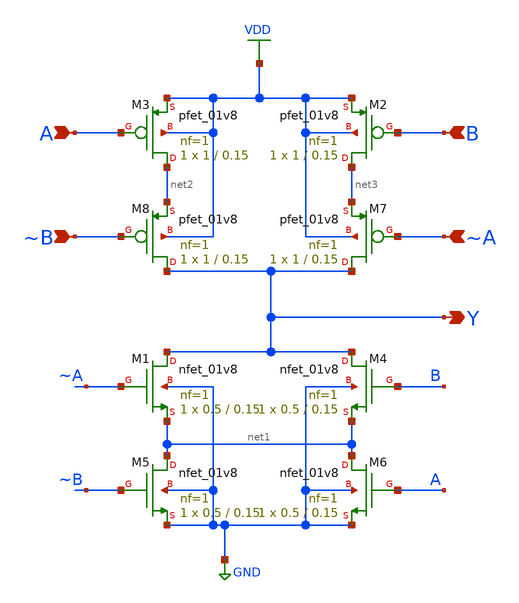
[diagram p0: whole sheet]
** sch_path: library/xschem/xor.sch
**.subckt xor Y A ~B B ~A
*.opin Y
*.ipin A
*.ipin ~B
*.ipin B
*.ipin ~A
XM1 Y ~A net1 GND sky130_fd_pr__nfet_01v8 L=0.15 W=0.5 nf=1 ad='int((nf+1)/2) * W/nf * 0.29' as='int((nf+2)/2) * W/nf * 0.29'
+ pd='2*int((nf+1)/2) * (W/nf + 0.29)' ps='2*int((nf+2)/2) * (W/nf + 0.29)' nrd='0.29 / W' nrs='0.29 / W'
+ sa=0 sb=0 sd=0 mult=1 m=1
XM2 net3 B VDD VDD sky130_fd_pr__pfet_01v8 L=0.15 W=1 nf=1 ad='int((nf+1)/2) * W/nf * 0.29' as='int((nf+2)/2) * W/nf * 0.29'
+ pd='2*int((nf+1)/2) * (W/nf + 0.29)' ps='2*int((nf+2)/2) * (W/nf + 0.29)' nrd='0.29 / W' nrs='0.29 / W'
+ sa=0 sb=0 sd=0 mult=1 m=1
XM3 net2 A VDD VDD sky130_fd_pr__pfet_01v8 L=0.15 W=1 nf=1 ad='int((nf+1)/2) * W/nf * 0.29' as='int((nf+2)/2) * W/nf * 0.29'
+ pd='2*int((nf+1)/2) * (W/nf + 0.29)' ps='2*int((nf+2)/2) * (W/nf + 0.29)' nrd='0.29 / W' nrs='0.29 / W'
+ sa=0 sb=0 sd=0 mult=1 m=1
XM4 Y B net1 GND sky130_fd_pr__nfet_01v8 L=0.15 W=0.5 nf=1 ad='int((nf+1)/2) * W/nf * 0.29' as='int((nf+2)/2) * W/nf * 0.29'
+ pd='2*int((nf+1)/2) * (W/nf + 0.29)' ps='2*int((nf+2)/2) * (W/nf + 0.29)' nrd='0.29 / W' nrs='0.29 / W'
+ sa=0 sb=0 sd=0 mult=1 m=1
XM5 net1 ~B GND GND sky130_fd_pr__nfet_01v8 L=0.15 W=0.5 nf=1 ad='int((nf+1)/2) * W/nf * 0.29' as='int((nf+2)/2) * W/nf * 0.29'
+ pd='2*int((nf+1)/2) * (W/nf + 0.29)' ps='2*int((nf+2)/2) * (W/nf + 0.29)' nrd='0.29 / W' nrs='0.29 / W'
+ sa=0 sb=0 sd=0 mult=1 m=1
XM6 net1 A GND GND sky130_fd_pr__nfet_01v8 L=0.15 W=0.5 nf=1 ad='int((nf+1)/2) * W/nf * 0.29' as='int((nf+2)/2) * W/nf * 0.29'
+ pd='2*int((nf+1)/2) * (W/nf + 0.29)' ps='2*int((nf+2)/2) * (W/nf + 0.29)' nrd='0.29 / W' nrs='0.29 / W'
+ sa=0 sb=0 sd=0 mult=1 m=1
XM7 Y ~A net3 VDD sky130_fd_pr__pfet_01v8 L=0.15 W=1 nf=1 ad='int((nf+1)/2) * W/nf * 0.29' as='int((nf+2)/2) * W/nf * 0.29'
+ pd='2*int((nf+1)/2) * (W/nf + 0.29)' ps='2*int((nf+2)/2) * (W/nf + 0.29)' nrd='0.29 / W' nrs='0.29 / W'
+ sa=0 sb=0 sd=0 mult=1 m=1
XM8 Y ~B net2 VDD sky130_fd_pr__pfet_01v8 L=0.15 W=1 nf=1 ad='int((nf+1)/2) * W/nf * 0.29' as='int((nf+2)/2) * W/nf * 0.29'
+ pd='2*int((nf+1)/2) * (W/nf + 0.29)' ps='2*int((nf+2)/2) * (W/nf + 0.29)' nrd='0.29 / W' nrs='0.29 / W'
+ sa=0 sb=0 sd=0 mult=1 m=1
**.ends
.GLOBAL VDD
.GLOBAL GND
.end
